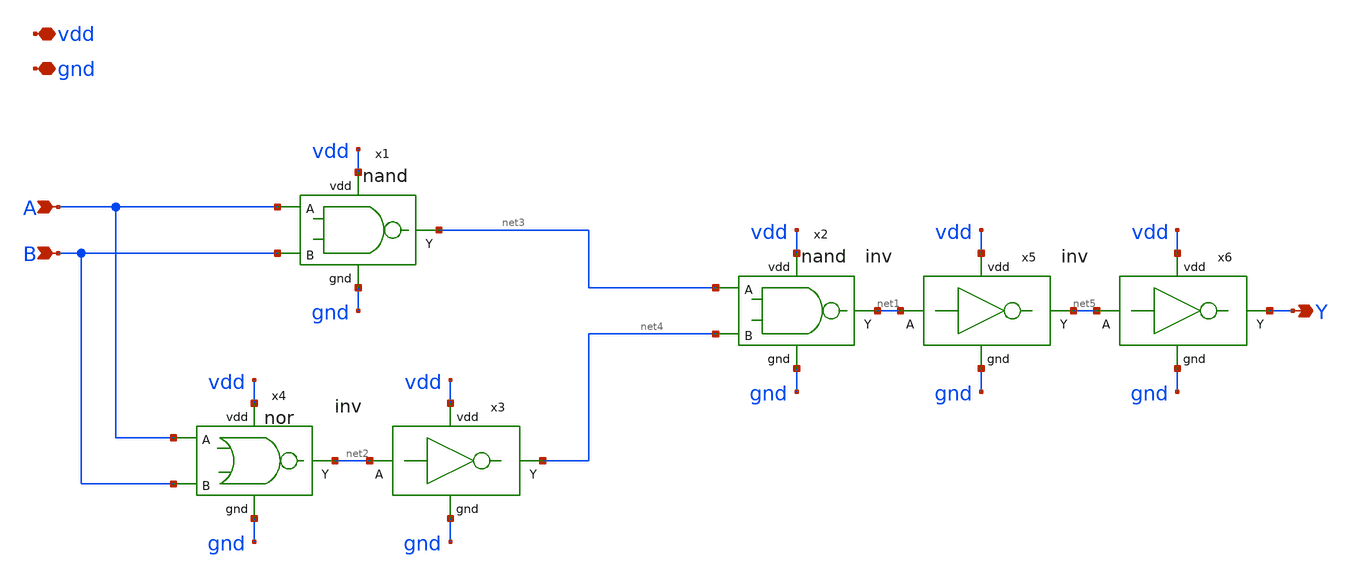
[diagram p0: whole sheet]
** sch_path: lab7/sch/XNOR.sch
**.subckt XNOR A B Y vdd gnd
*.ipin A
*.ipin B
*.opin Y
*.iopin vdd
*.iopin gnd
x1 A B net3 vdd gnd nand
x2 net3 net4 net1 vdd gnd nand
x4 A B net2 vdd gnd nor
x5 net1 net5 vdd gnd inv
x3 net2 net4 vdd gnd inv
x6 net5 Y vdd gnd inv
**.ends

* expanding   symbol:  /home/dayesong/ETRI050_DesignKit/lab7/sch/nand.sym # of pins=5
** sym_path: lab7/sch/nand.sym
** sch_path: lab7/sch/nand.sch
.subckt nand A B Y vdd gnd
*.ipin A
*.ipin B
*.opin Y
*.iopin vdd
*.iopin gnd
M3 net1 A gnd gnd nfet w=6u l=0.6u m=1
M4 Y B vdd vdd pfet w=6u l=0.6u m=1
M2 Y A vdd vdd pfet w=6u l=0.6u m=1
M1 Y B net1 gnd nfet w=6u l=0.6u m=1
.ends


* expanding   symbol:  /home/dayesong/ETRI050_DesignKit/lab7/sch/nor.sym # of pins=5
** sym_path: lab7/sch/nor.sym
** sch_path: lab7/sch/nor.sch
.subckt nor A B Y vdd gnd
*.ipin A
*.ipin B
*.opin Y
*.iopin vdd
*.iopin gnd
M3 net1 A vdd vdd pfet w=12u l=0.6u m=1
M4 Y A gnd gnd nfet w=3u l=0.6u m=1
M1 Y B gnd gnd nfet w=3u l=0.6u m=1
M2 Y B net1 vdd pfet w=12u l=0.6u m=1
.ends


* expanding   symbol:  /home/dayesong/ETRI050_DesignKit/lab7/sch/inv.sym # of pins=4
** sym_path: lab7/sch/inv.sym
** sch_path: lab7/sch/inv.sch
.subckt inv A Y vdd gnd
*.ipin A
*.opin Y
*.iopin vdd
*.iopin gnd
M1 Y A vdd vdd pfet w=6u l=0.6u m=1
M2 Y A gnd gnd nfet w=3u l=0.6u m=1
.ends

.end
